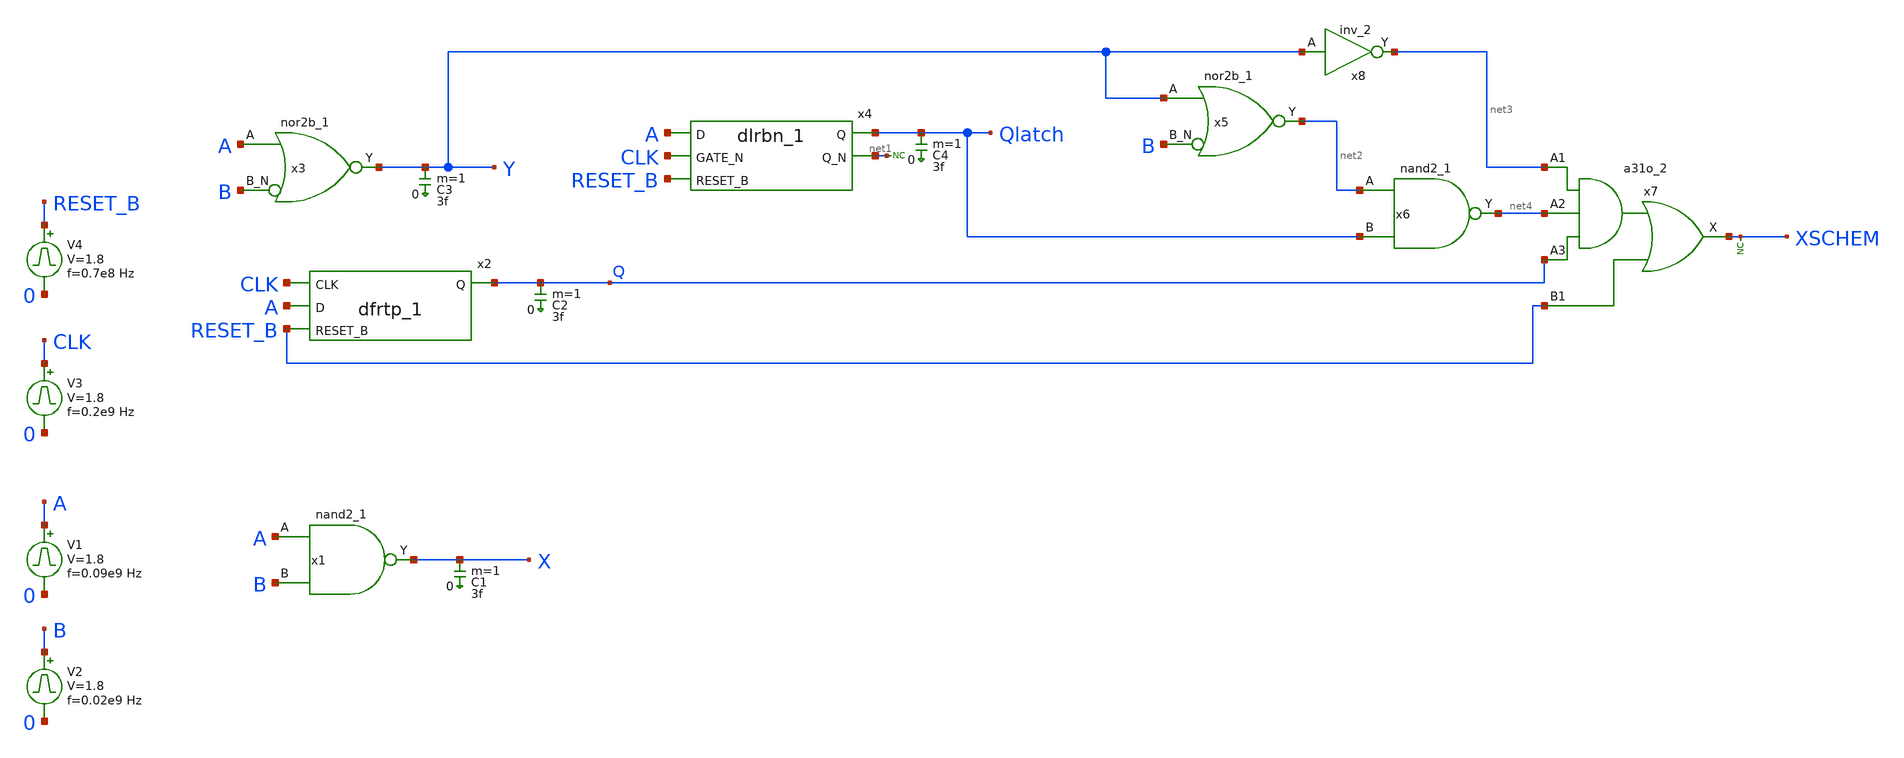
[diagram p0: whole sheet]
** sch_path: sky130_tests/test_stdcells.sch
* Copyright 2021 Stefan Frederik Schippers
* Licensed under the Apache License, Version 2.0 (the "License");
* you may not use this file except in compliance with the License.
* You may obtain a copy of the License at
* https://www.apache.org/licenses/LICENSE-2.0
* Unless required by applicable law or agreed to in writing, software
* distributed under the License is distributed on an "AS IS" BASIS,
* WITHOUT WARRANTIES OR CONDITIONS OF ANY KIND, either express or implied.
* See the License for the specific language governing permissions and
* limitations under the License.
**.subckt test_stdcells
x1 A B VSS VSS VCC VCC X sky130_fd_sc_hd__nand2_1
V1 A 0 pulse 0 1.8 '0.495/ 0.09e9 ' '0.01/0.09e9 ' '0.01/0.09e9 ' '0.49/0.09e9 ' '1/0.09e9 '
V2 B 0 pulse 0 1.8 '0.495/ 0.02e9 ' '0.01/0.02e9 ' '0.01/0.02e9 ' '0.49/0.02e9 ' '1/0.02e9 '
C1 X 0 3f m=1
x2 CLK A RESET_B VSS VSS VCC VCC Q sky130_fd_sc_hd__dfrtp_1
V3 CLK 0 pulse 0 1.8 '0.495/ 0.2e9 ' '0.01/0.2e9 ' '0.01/0.2e9 ' '0.49/0.2e9 ' '1/0.2e9 '
V4 RESET_B 0 pulse 0 1.8 '0.495/ 0.7e8 ' '0.01/0.7e8 ' '0.01/0.7e8 ' '0.49/0.7e8 ' '1/0.7e8 '
C2 Q 0 3f m=1
C3 Y 0 3f m=1
x3 A B VSS VSS VCC VCC Y sky130_fd_sc_hd__nor2b_1
x4 A CLK RESET_B VSS VSS VCC VCC Qlatch net1 sky130_fd_sc_hd__dlrbn_1
C4 Qlatch 0 3f m=1
x5 Y B VSS VSS VCC VCC net2 sky130_fd_sc_hd__nor2b_1
x6 net2 Qlatch VSS VSS VCC VCC net4 sky130_fd_sc_hd__nand2_1
x7 net3 net4 Q RESET_B VSS VSS VCC VCC XSCHEM sky130_fd_sc_hd__a31o_2
* noconn #net1
* noconn XSCHEM
x8 Y VSS VSS VCC VCC net3 sky130_fd_sc_hd__inv_2
**** begin user architecture code


.options acct list
.temp 25
vvcc vcc 0 dc 1.8
vvss vss 0 0
.control
tran 30p 80n
plot a b+2 clk+4 reset_b+6 x+8 y+10 q+12 qlatch+14
.endc


 .lib $::SKYWATER_MODELS/sky130.lib.spice tt
.include $::SKYWATER_STDCELLS/sky130_fd_sc_hd.spice
.param mc_mm_switch=0
.param mc_pr_switch=0

**** end user architecture code
**.ends
.end
